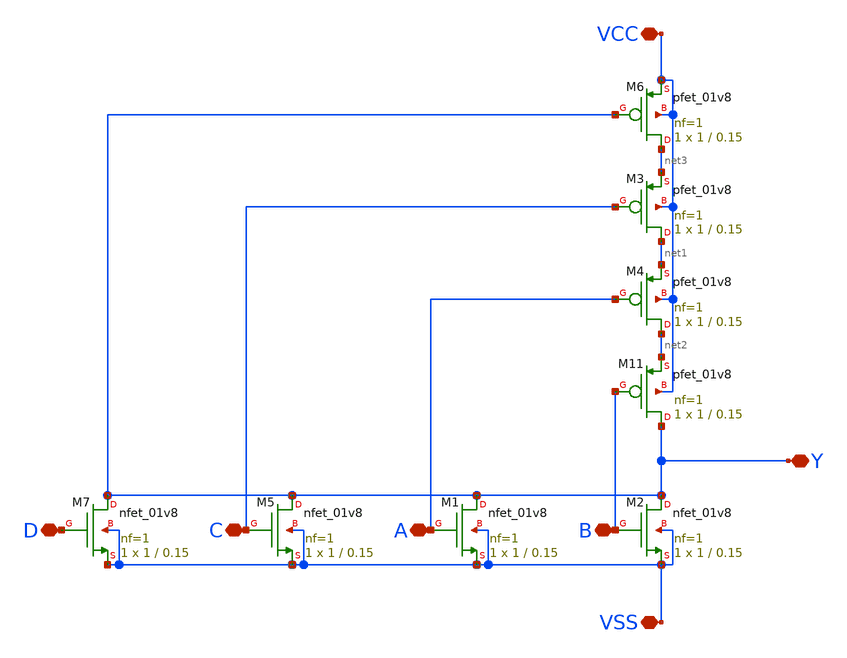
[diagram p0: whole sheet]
** sch_path: logic gates/nor4.sch
**.subckt nor4 VSS Y A B C VCC D
*.iopin VSS
*.iopin Y
*.iopin A
*.iopin B
*.iopin C
*.iopin VCC
*.iopin D
XM2 Y B VSS VSS sky130_fd_pr__nfet_01v8 L=0.15 W=1 nf=1 ad='int((1 + 1)/2) * 1 / 1 * 0.29' as='int((1 + 2)/2) * 1 / 1 * 0.29'
+ pd='2*int((1 + 1)/2) * (1 / 1 + 0.29)' ps='2*int((1 + 2)/2) * (1 / 1 + 0.29)' nrd='0.29 / 1 ' nrs='0.29 / 1 '
+ sa=0 sb=0 sd=0 mult=1 m=1
XM11 Y B net2 VCC sky130_fd_pr__pfet_01v8 L=0.15 W=1 nf=1 ad='int((nf+1)/2) * W/nf * 0.29' as='int((nf+2)/2) * W/nf * 0.29'
+ pd='2*int((nf+1)/2) * (W/nf + 0.29)' ps='2*int((nf+2)/2) * (W/nf + 0.29)' nrd='0.29 / W' nrs='0.29 / W'
+ sa=0 sb=0 sd=0 mult=1 m=1
XM1 Y A VSS VSS sky130_fd_pr__nfet_01v8 L=0.15 W=1 nf=1 ad='int((1 + 1)/2) * 1 / 1 * 0.29' as='int((1 + 2)/2) * 1 / 1 * 0.29'
+ pd='2*int((1 + 1)/2) * (1 / 1 + 0.29)' ps='2*int((1 + 2)/2) * (1 / 1 + 0.29)' nrd='0.29 / 1 ' nrs='0.29 / 1 '
+ sa=0 sb=0 sd=0 mult=1 m=1
XM3 net1 C net3 VCC sky130_fd_pr__pfet_01v8 L=0.15 W=1 nf=1 ad='int((nf+1)/2) * W/nf * 0.29' as='int((nf+2)/2) * W/nf * 0.29'
+ pd='2*int((nf+1)/2) * (W/nf + 0.29)' ps='2*int((nf+2)/2) * (W/nf + 0.29)' nrd='0.29 / W' nrs='0.29 / W'
+ sa=0 sb=0 sd=0 mult=1 m=1
XM4 net2 A net1 VCC sky130_fd_pr__pfet_01v8 L=0.15 W=1 nf=1 ad='int((nf+1)/2) * W/nf * 0.29' as='int((nf+2)/2) * W/nf * 0.29'
+ pd='2*int((nf+1)/2) * (W/nf + 0.29)' ps='2*int((nf+2)/2) * (W/nf + 0.29)' nrd='0.29 / W' nrs='0.29 / W'
+ sa=0 sb=0 sd=0 mult=1 m=1
XM5 Y C VSS VSS sky130_fd_pr__nfet_01v8 L=0.15 W=1 nf=1 ad='int((1 + 1)/2) * 1 / 1 * 0.29' as='int((1 + 2)/2) * 1 / 1 * 0.29'
+ pd='2*int((1 + 1)/2) * (1 / 1 + 0.29)' ps='2*int((1 + 2)/2) * (1 / 1 + 0.29)' nrd='0.29 / 1 ' nrs='0.29 / 1 '
+ sa=0 sb=0 sd=0 mult=1 m=1
XM6 net3 Y VCC VCC sky130_fd_pr__pfet_01v8 L=0.15 W=1 nf=1 ad='int((nf+1)/2) * W/nf * 0.29' as='int((nf+2)/2) * W/nf * 0.29'
+ pd='2*int((nf+1)/2) * (W/nf + 0.29)' ps='2*int((nf+2)/2) * (W/nf + 0.29)' nrd='0.29 / W' nrs='0.29 / W'
+ sa=0 sb=0 sd=0 mult=1 m=1
XM7 Y D VSS VSS sky130_fd_pr__nfet_01v8 L=0.15 W=1 nf=1 ad='int((1 + 1)/2) * 1 / 1 * 0.29' as='int((1 + 2)/2) * 1 / 1 * 0.29'
+ pd='2*int((1 + 1)/2) * (1 / 1 + 0.29)' ps='2*int((1 + 2)/2) * (1 / 1 + 0.29)' nrd='0.29 / 1 ' nrs='0.29 / 1 '
+ sa=0 sb=0 sd=0 mult=1 m=1
**.ends
.end
